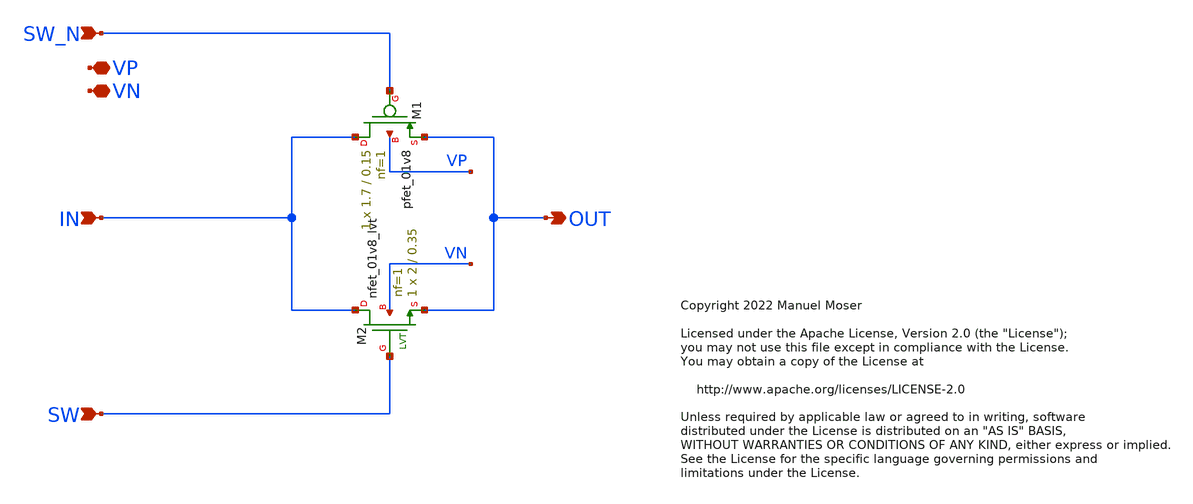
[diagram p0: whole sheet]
** sch_path: xschem/switch/switch_150n.sch
* Copyright 2022 Manuel Moser
* Licensed under the Apache License, Version 2.0 (the "License");
**.subckt switch_150n VN VP IN OUT SW_N SW
*.iopin VN
*.iopin VP
*.ipin IN
*.opin OUT
*.ipin SW_N
*.ipin SW
XM2 IN SW OUT VN sky130_fd_pr__nfet_01v8_lvt L=0.35 W=2 nf=1 ad='int((nf+1)/2) * W/nf * 0.29' as='int((nf+2)/2) * W/nf * 0.29'
+ pd='2*int((nf+1)/2) * (W/nf + 0.29)' ps='2*int((nf+2)/2) * (W/nf + 0.29)' nrd='0.29 / W' nrs='0.29 / W'
+ sa=0 sb=0 sd=0 mult=1 m=1
XM1 IN SW_N OUT VP sky130_fd_pr__pfet_01v8 L=0.15 W=1.7 nf=1 ad='int((nf+1)/2) * W/nf * 0.29' as='int((nf+2)/2) * W/nf * 0.29'
+ pd='2*int((nf+1)/2) * (W/nf + 0.29)' ps='2*int((nf+2)/2) * (W/nf + 0.29)' nrd='0.29 / W' nrs='0.29 / W'
+ sa=0 sb=0 sd=0 mult=1 m=1
**.ends
.end
